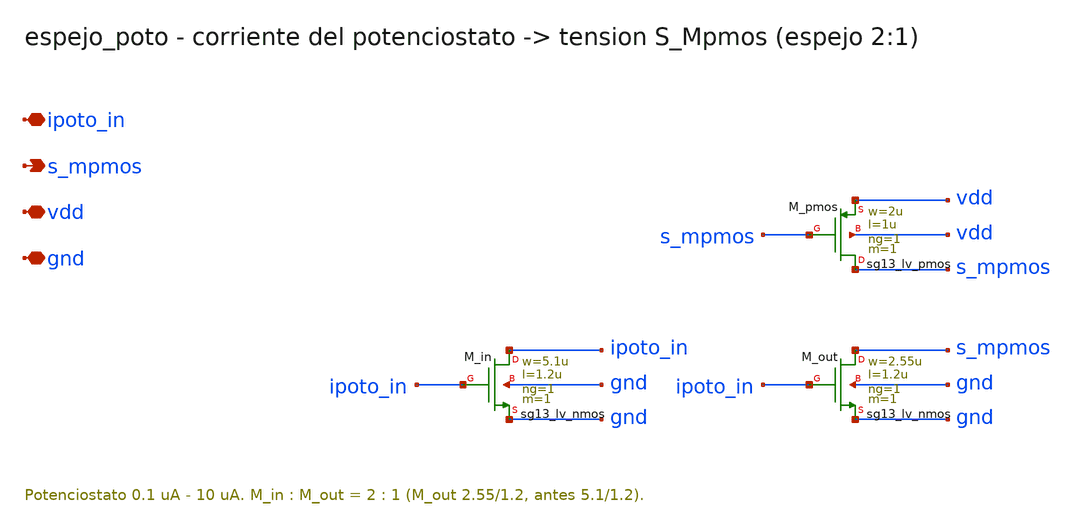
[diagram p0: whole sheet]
** sch_path: Enfoque_B/xschem/celdas/espejo_poto.sch
**.subckt espejo_poto ipoto_in s_mpmos vdd gnd
*.iopin ipoto_in
*.opin s_mpmos
*.iopin vdd
*.iopin gnd
XM_in ipoto_in ipoto_in gnd gnd sg13_lv_nmos w=5.1u l=1.2u ng=1 m=1 mm_ok=1
XM_out s_mpmos ipoto_in gnd gnd sg13_lv_nmos w=2.55u l=1.2u ng=1 m=1 mm_ok=1
XM_pmos s_mpmos s_mpmos vdd vdd sg13_lv_pmos w=2u l=1u ng=1 m=1 mm_ok=1
**.ends
.end
